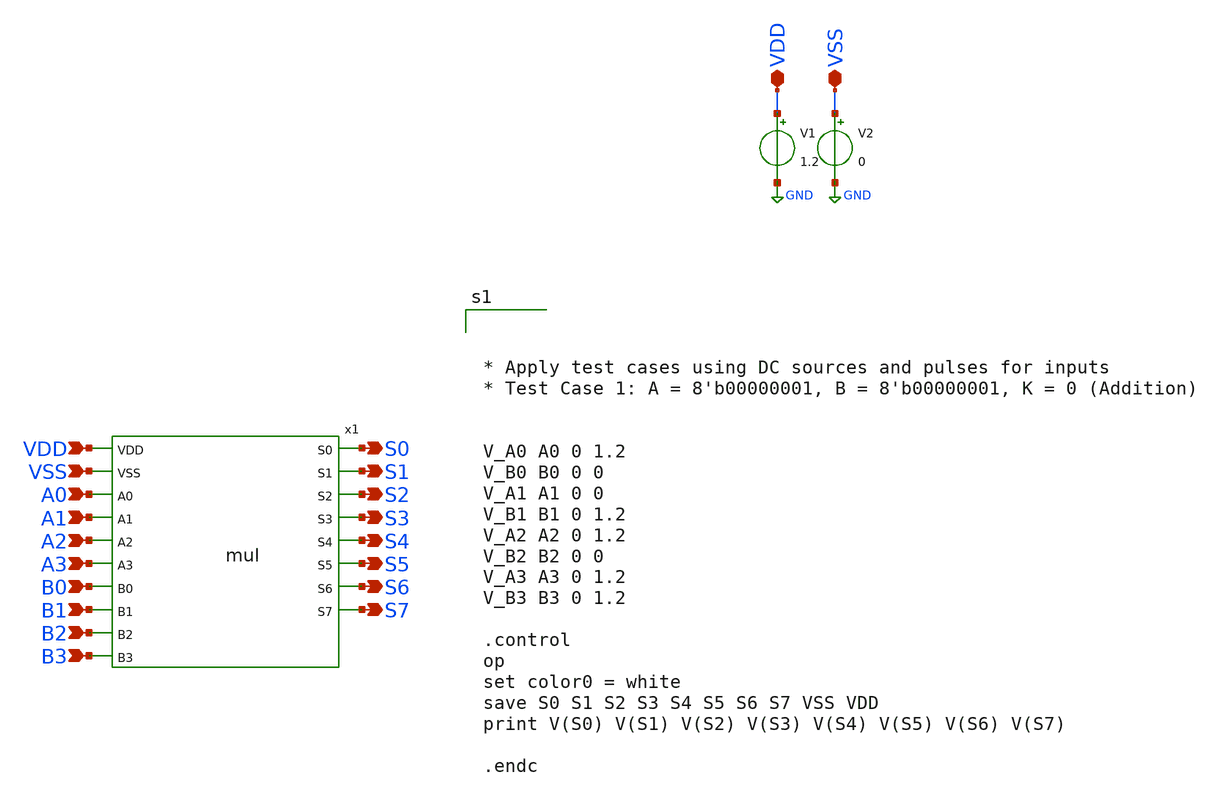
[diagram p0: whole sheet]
** sch_path: design/xschem/TEST_BENCHES/MULTIPLIER_TB.sch
**.subckt MULTIPLIER_TB VDD VSS A0 A1 A2 A3 B1 B2 B3 B0 S6 S7 S3 S4 S5 S0 S1 S2 VDD VSS
*.iopin VDD
*.iopin VSS
*.ipin A0
*.ipin A1
*.ipin A2
*.ipin A3
*.ipin B1
*.ipin B2
*.ipin B3
*.ipin B0
*.opin S6
*.opin S7
*.opin S3
*.opin S4
*.opin S5
*.opin S0
*.opin S1
*.opin S2
*.ipin VDD
*.ipin VSS
V1 VDD GND 1.2
V2 VSS GND 0
x1 VDD VSS A0 A1 A2 A3 B0 B1 B2 B3 S0 S1 S2 S5 S4 S3 S7 S6 VSS VDD mul
**** begin user architecture code

** opencircuitdesign pdks install
.lib $::SKYWATER_MODELS/sky130.lib.spice tt_mm





* Apply test cases using DC sources and pulses for inputs
* Test Case 1: A = 8'b00000001, B = 8'b00000001, K = 0 (Addition)


V_A0 A0 0 1.2
V_B0 B0 0 0
V_A1 A1 0 0
V_B1 B1 0 1.2
V_A2 A2 0 1.2
V_B2 B2 0 0
V_A3 A3 0 1.2
V_B3 B3 0 1.2

.control
op
set color0 = white
save S0 S1 S2 S3 S4 S5 S6 S7 VSS VDD
print V(S0) V(S1) V(S2) V(S3) V(S4) V(S5) V(S6) V(S7)

.endc


**** end user architecture code
**.ends
.GLOBAL GND
.end
